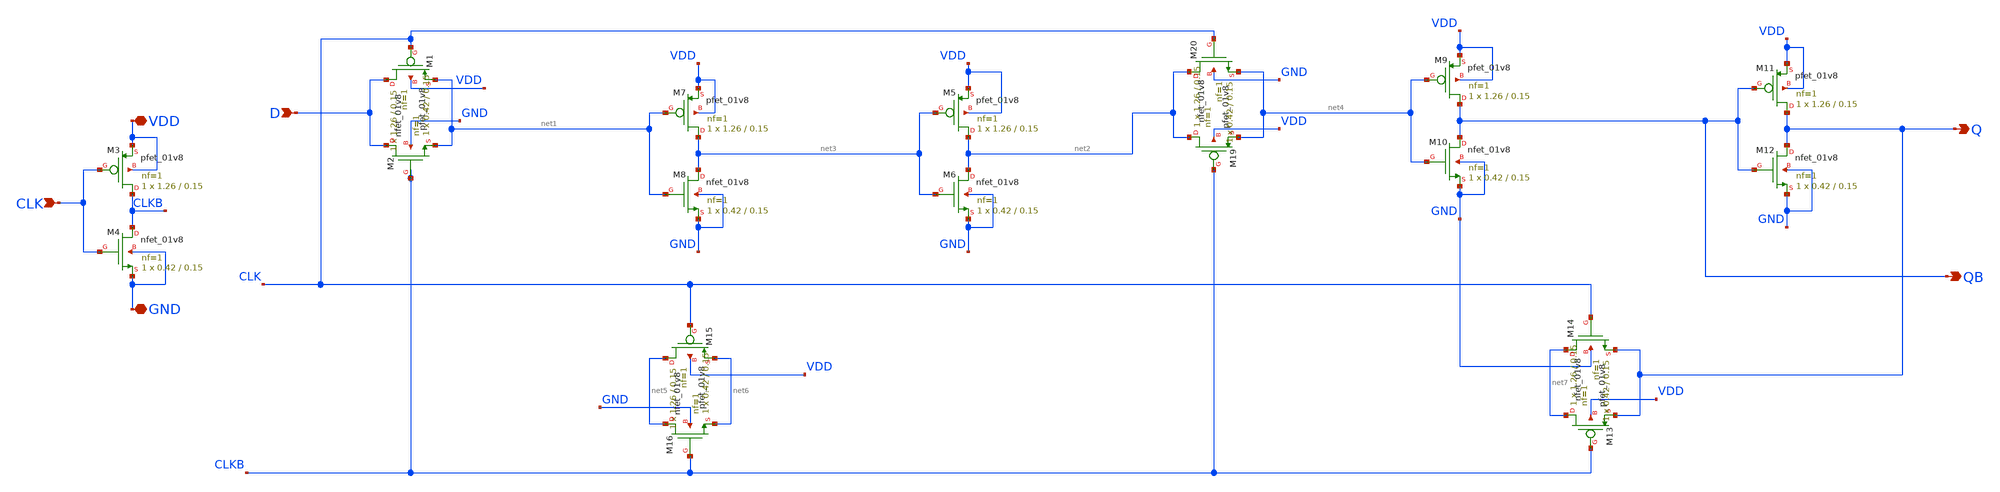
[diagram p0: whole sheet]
** sch_path: cells/DFFX1/schematic/dffx1.sch
**.subckt dffx1 VDD GND CLK D Q QB
*.iopin VDD
*.iopin GND
*.ipin CLK
*.ipin D
*.opin Q
*.opin QB
XM1 D CLK net1 VDD sky130_fd_pr__pfet_01v8 L=0.15 W=1.26 nf=1 ad='int((1 + 1)/2) * 1.26 / 1 * 0.29' as='int((1 + 2)/2) * 1.26 / 1 * 0.29'
+ pd='2*int((1 + 1)/2) * (1.26 / 1 + 0.29)' ps='2*int((1 + 2)/2) * (1.26 / 1 + 0.29)' nrd='0.29 / 1.26 '
+ nrs='0.29 / 1.26 ' sa=0 sb=0 sd=0 mult=1 m=1
XM2 D CLKB net1 GND sky130_fd_pr__nfet_01v8 L=0.15 W=0.42 nf=1 ad='int((1 + 1)/2) * 0.42 / 1 * 0.29'
+ as='int((1 + 2)/2) * 0.42 / 1 * 0.29' pd='2*int((1 + 1)/2) * (0.42 / 1 + 0.29)' ps='2*int((1 + 2)/2) * (0.42 / 1 + 0.29)'
+ nrd='0.29 / 0.42 ' nrs='0.29 / 0.42 ' sa=0 sb=0 sd=0 mult=1 m=1
XM3 CLKB CLK VDD VDD sky130_fd_pr__pfet_01v8 L=0.15 W=1.26 nf=1 ad='int((1 + 1)/2) * 1.26 / 1 * 0.29'
+ as='int((1 + 2)/2) * 1.26 / 1 * 0.29' pd='2*int((1 + 1)/2) * (1.26 / 1 + 0.29)' ps='2*int((1 + 2)/2) * (1.26 / 1 + 0.29)'
+ nrd='0.29 / 1.26 ' nrs='0.29 / 1.26 ' sa=0 sb=0 sd=0 mult=1 m=1
XM4 CLKB CLK GND GND sky130_fd_pr__nfet_01v8 L=0.15 W=0.42 nf=1 ad='int((1 + 1)/2) * 0.42 / 1 * 0.29'
+ as='int((1 + 2)/2) * 0.42 / 1 * 0.29' pd='2*int((1 + 1)/2) * (0.42 / 1 + 0.29)' ps='2*int((1 + 2)/2) * (0.42 / 1 + 0.29)'
+ nrd='0.29 / 0.42 ' nrs='0.29 / 0.42 ' sa=0 sb=0 sd=0 mult=1 m=1
XM5 net2 net3 VDD VDD sky130_fd_pr__pfet_01v8 L=0.15 W=1.26 nf=1 ad='int((1 + 1)/2) * 1.26 / 1 * 0.29'
+ as='int((1 + 2)/2) * 1.26 / 1 * 0.29' pd='2*int((1 + 1)/2) * (1.26 / 1 + 0.29)' ps='2*int((1 + 2)/2) * (1.26 / 1 + 0.29)'
+ nrd='0.29 / 1.26 ' nrs='0.29 / 1.26 ' sa=0 sb=0 sd=0 mult=1 m=1
XM6 net2 net3 GND GND sky130_fd_pr__nfet_01v8 L=0.15 W=0.42 nf=1 ad='int((1 + 1)/2) * 0.42 / 1 * 0.29'
+ as='int((1 + 2)/2) * 0.42 / 1 * 0.29' pd='2*int((1 + 1)/2) * (0.42 / 1 + 0.29)' ps='2*int((1 + 2)/2) * (0.42 / 1 + 0.29)'
+ nrd='0.29 / 0.42 ' nrs='0.29 / 0.42 ' sa=0 sb=0 sd=0 mult=1 m=1
XM7 net3 net1 VDD VDD sky130_fd_pr__pfet_01v8 L=0.15 W=1.26 nf=1 ad='int((1 + 1)/2) * 1.26 / 1 * 0.29'
+ as='int((1 + 2)/2) * 1.26 / 1 * 0.29' pd='2*int((1 + 1)/2) * (1.26 / 1 + 0.29)' ps='2*int((1 + 2)/2) * (1.26 / 1 + 0.29)'
+ nrd='0.29 / 1.26 ' nrs='0.29 / 1.26 ' sa=0 sb=0 sd=0 mult=1 m=1
XM8 net3 net1 GND GND sky130_fd_pr__nfet_01v8 L=0.15 W=0.42 nf=1 ad='int((1 + 1)/2) * 0.42 / 1 * 0.29'
+ as='int((1 + 2)/2) * 0.42 / 1 * 0.29' pd='2*int((1 + 1)/2) * (0.42 / 1 + 0.29)' ps='2*int((1 + 2)/2) * (0.42 / 1 + 0.29)'
+ nrd='0.29 / 0.42 ' nrs='0.29 / 0.42 ' sa=0 sb=0 sd=0 mult=1 m=1
XM9 QB net4 VDD VDD sky130_fd_pr__pfet_01v8 L=0.15 W=1.26 nf=1 ad='int((1 + 1)/2) * 1.26 / 1 * 0.29'
+ as='int((1 + 2)/2) * 1.26 / 1 * 0.29' pd='2*int((1 + 1)/2) * (1.26 / 1 + 0.29)' ps='2*int((1 + 2)/2) * (1.26 / 1 + 0.29)'
+ nrd='0.29 / 1.26 ' nrs='0.29 / 1.26 ' sa=0 sb=0 sd=0 mult=1 m=1
XM10 QB net4 GND GND sky130_fd_pr__nfet_01v8 L=0.15 W=0.42 nf=1 ad='int((1 + 1)/2) * 0.42 / 1 * 0.29'
+ as='int((1 + 2)/2) * 0.42 / 1 * 0.29' pd='2*int((1 + 1)/2) * (0.42 / 1 + 0.29)' ps='2*int((1 + 2)/2) * (0.42 / 1 + 0.29)'
+ nrd='0.29 / 0.42 ' nrs='0.29 / 0.42 ' sa=0 sb=0 sd=0 mult=1 m=1
XM11 Q QB VDD VDD sky130_fd_pr__pfet_01v8 L=0.15 W=1.26 nf=1 ad='int((1 + 1)/2) * 1.26 / 1 * 0.29' as='int((1 + 2)/2) * 1.26 / 1 * 0.29'
+ pd='2*int((1 + 1)/2) * (1.26 / 1 + 0.29)' ps='2*int((1 + 2)/2) * (1.26 / 1 + 0.29)' nrd='0.29 / 1.26 '
+ nrs='0.29 / 1.26 ' sa=0 sb=0 sd=0 mult=1 m=1
XM12 Q QB GND GND sky130_fd_pr__nfet_01v8 L=0.15 W=0.42 nf=1 ad='int((1 + 1)/2) * 0.42 / 1 * 0.29' as='int((1 + 2)/2) * 0.42 / 1 * 0.29'
+ pd='2*int((1 + 1)/2) * (0.42 / 1 + 0.29)' ps='2*int((1 + 2)/2) * (0.42 / 1 + 0.29)' nrd='0.29 / 0.42 '
+ nrs='0.29 / 0.42 ' sa=0 sb=0 sd=0 mult=1 m=1
XM13 net7 CLKB Q VDD sky130_fd_pr__pfet_01v8 L=0.15 W=1.26 nf=1 ad='int((1 + 1)/2) * 1.26 / 1 * 0.29'
+ as='int((1 + 2)/2) * 1.26 / 1 * 0.29' pd='2*int((1 + 1)/2) * (1.26 / 1 + 0.29)' ps='2*int((1 + 2)/2) * (1.26 / 1 + 0.29)'
+ nrd='0.29 / 1.26 ' nrs='0.29 / 1.26 ' sa=0 sb=0 sd=0 mult=1 m=1
XM14 net7 CLK Q GND sky130_fd_pr__nfet_01v8 L=0.15 W=0.42 nf=1 ad='int((1 + 1)/2) * 0.42 / 1 * 0.29'
+ as='int((1 + 2)/2) * 0.42 / 1 * 0.29' pd='2*int((1 + 1)/2) * (0.42 / 1 + 0.29)' ps='2*int((1 + 2)/2) * (0.42 / 1 + 0.29)'
+ nrd='0.29 / 0.42 ' nrs='0.29 / 0.42 ' sa=0 sb=0 sd=0 mult=1 m=1
XM15 net5 CLK net6 VDD sky130_fd_pr__pfet_01v8 L=0.15 W=1.26 nf=1 ad='int((1 + 1)/2) * 1.26 / 1 * 0.29'
+ as='int((1 + 2)/2) * 1.26 / 1 * 0.29' pd='2*int((1 + 1)/2) * (1.26 / 1 + 0.29)' ps='2*int((1 + 2)/2) * (1.26 / 1 + 0.29)'
+ nrd='0.29 / 1.26 ' nrs='0.29 / 1.26 ' sa=0 sb=0 sd=0 mult=1 m=1
XM16 net5 CLKB net6 GND sky130_fd_pr__nfet_01v8 L=0.15 W=0.42 nf=1 ad='int((1 + 1)/2) * 0.42 / 1 * 0.29'
+ as='int((1 + 2)/2) * 0.42 / 1 * 0.29' pd='2*int((1 + 1)/2) * (0.42 / 1 + 0.29)' ps='2*int((1 + 2)/2) * (0.42 / 1 + 0.29)'
+ nrd='0.29 / 0.42 ' nrs='0.29 / 0.42 ' sa=0 sb=0 sd=0 mult=1 m=1
XM19 net2 CLKB net4 VDD sky130_fd_pr__pfet_01v8 L=0.15 W=1.26 nf=1 ad='int((1 + 1)/2) * 1.26 / 1 * 0.29'
+ as='int((1 + 2)/2) * 1.26 / 1 * 0.29' pd='2*int((1 + 1)/2) * (1.26 / 1 + 0.29)' ps='2*int((1 + 2)/2) * (1.26 / 1 + 0.29)'
+ nrd='0.29 / 1.26 ' nrs='0.29 / 1.26 ' sa=0 sb=0 sd=0 mult=1 m=1
XM20 net2 CLK net4 GND sky130_fd_pr__nfet_01v8 L=0.15 W=0.42 nf=1 ad='int((1 + 1)/2) * 0.42 / 1 * 0.29'
+ as='int((1 + 2)/2) * 0.42 / 1 * 0.29' pd='2*int((1 + 1)/2) * (0.42 / 1 + 0.29)' ps='2*int((1 + 2)/2) * (0.42 / 1 + 0.29)'
+ nrd='0.29 / 0.42 ' nrs='0.29 / 0.42 ' sa=0 sb=0 sd=0 mult=1 m=1
**.ends
.end
